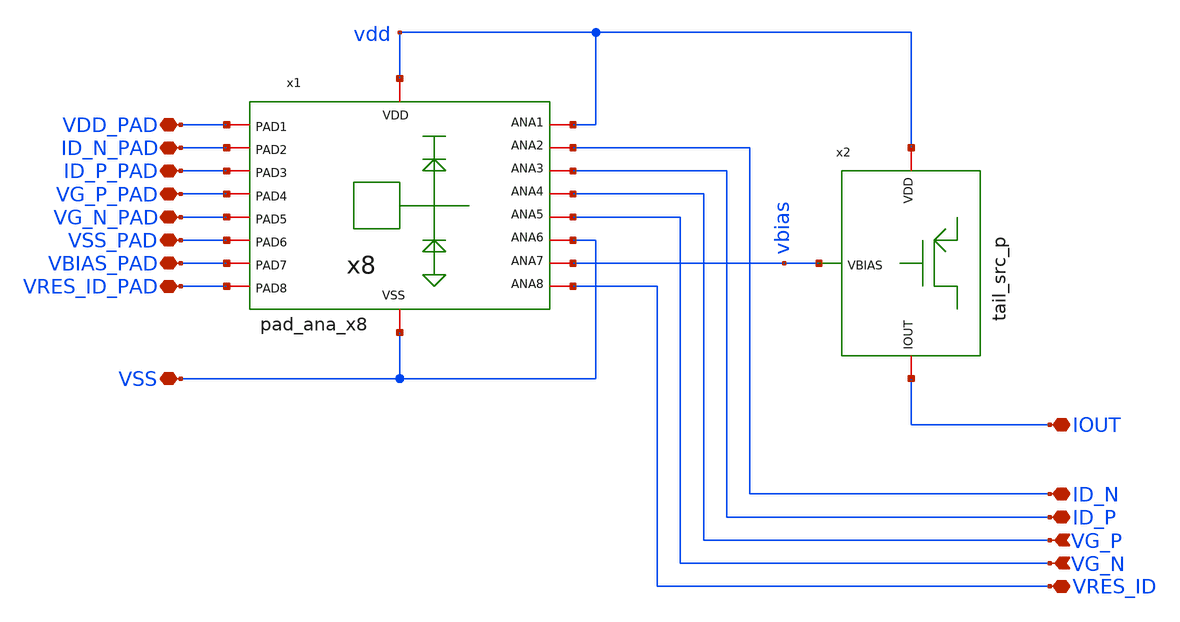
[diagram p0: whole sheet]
** sch_path: JKU_TC1/design_data/sfl-test-cells/xschem/testcells/tb_pmos.sch
**.subckt tb_pmos VDD_PAD ID_N_PAD ID_P_PAD VG_P_PAD VG_N_PAD VSS_PAD VBIAS_PAD VRES_ID_PAD VSS IOUT
*+ VRES_ID ID_N ID_P VG_P VG_N
*.iopin VDD_PAD
*.iopin ID_N_PAD
*.iopin ID_P_PAD
*.iopin VG_P_PAD
*.iopin VG_N_PAD
*.iopin VSS_PAD
*.iopin VBIAS_PAD
*.iopin VRES_ID_PAD
*.iopin VSS
*.iopin IOUT
*.iopin VRES_ID
*.iopin ID_N
*.iopin ID_P
*.ipin VG_P
*.ipin VG_N
x1 VSS_PAD VDD_PAD VG_P_PAD VG_N_PAD ID_N_PAD ID_P_PAD VBIAS_PAD VRES_ID_PAD vdd VSS VG_N VG_P
+ VRES_ID ID_P vbias VSS ID_N vdd pad_ana_x8
x2 vdd vbias IOUT tail_src_p
**.ends

* expanding   symbol:  pads/pad_ana_x8.sym # of pins=18
** sym_path: JKU_TC1/design_data/xschem/pads/pad_ana_x8.sym
** sch_path: JKU_TC1/design_data/xschem/pads/pad_ana_x8.sch
.subckt pad_ana_x8 PAD6 PAD1 PAD4 PAD5 PAD2 PAD3 PAD7 PAD8 VDD VSS ANA5 ANA4 ANA8 ANA3 ANA7 ANA6
+ ANA2 ANA1
*.iopin VDD
*.iopin VSS
*.iopin ANA1
*.iopin ANA2
*.iopin ANA3
*.iopin ANA4
*.iopin ANA5
*.iopin ANA6
*.iopin ANA7
*.iopin ANA8
*.iopin PAD1
*.iopin PAD2
*.iopin PAD3
*.iopin PAD4
*.iopin PAD5
*.iopin PAD6
*.iopin PAD7
*.iopin PAD8
xpad1 VDD PAD1 ANA1 VSS pad_ana
xpad2 VDD PAD2 ANA2 VSS pad_ana
xpad3 VDD PAD3 ANA3 VSS pad_ana
xpad4 VDD PAD4 ANA4 VSS pad_ana
xpad5 VDD PAD5 ANA5 VSS pad_ana
xpad6 VDD PAD6 ANA6 VSS pad_ana
xpad7 VDD PAD7 ANA7 VSS pad_ana
xpad8 VDD PAD8 ANA8 VSS pad_ana
.ends


* expanding   symbol:  tailsrcs/tail_src_p.sym # of pins=3
** sym_path: JKU_TC1/design_data/sfl-test-cells/xschem/tailsrcs/tail_src_p.sym
** sch_path: JKU_TC1/design_data/sfl-test-cells/xschem/tailsrcs/tail_src_p.sch
.subckt tail_src_p VDD VBIAS IOUT
*.ipin VBIAS
*.iopin VDD
*.iopin IOUT
XM1 IOUT VBIAS VDD VDD sg13_lv_pmos w=320u l=10u ng=40 m=5 mm_ok=1
XM2 VDD VBIAS VDD VDD sg13_lv_pmos w=8u l=10u ng=1 m=10 mm_ok=1
XM3 VDD VBIAS VDD VDD sg13_lv_pmos w=336u l=10u ng=42 m=2 mm_ok=1
.ends


* expanding   symbol:  pads/pad_ana.sym # of pins=4
** sym_path: JKU_TC1/design_data/xschem/pads/pad_ana.sym
** sch_path: JKU_TC1/design_data/xschem/pads/pad_ana.sch
.subckt pad_ana VDD PAD ANA VSS
*.iopin VSS
*.iopin PAD
*.iopin VDD
*.iopin ANA
XC1 VDD PAD cparasitic C=20f
XC2 PAD VSS cparasitic C=20f
R1 PAD ANA 1e-6 m=1
R2 PAD ANA 1e-6 m=1
xesd1 VDD PAD VSS pad_diodes
.ends


* expanding   symbol:  pads/pad_diodes.sym # of pins=3
** sym_path: JKU_TC1/design_data/xschem/pads/pad_diodes.sym
** sch_path: JKU_TC1/design_data/xschem/pads/pad_diodes.sch
.subckt pad_diodes VDD PAD VSS
*.iopin VDD
*.iopin VSS
*.iopin PAD
XXD1 PAD VDD dantenna l=780n w=780n
XXD2 VSS PAD dantenna l=780n w=780n
.ends

.end
